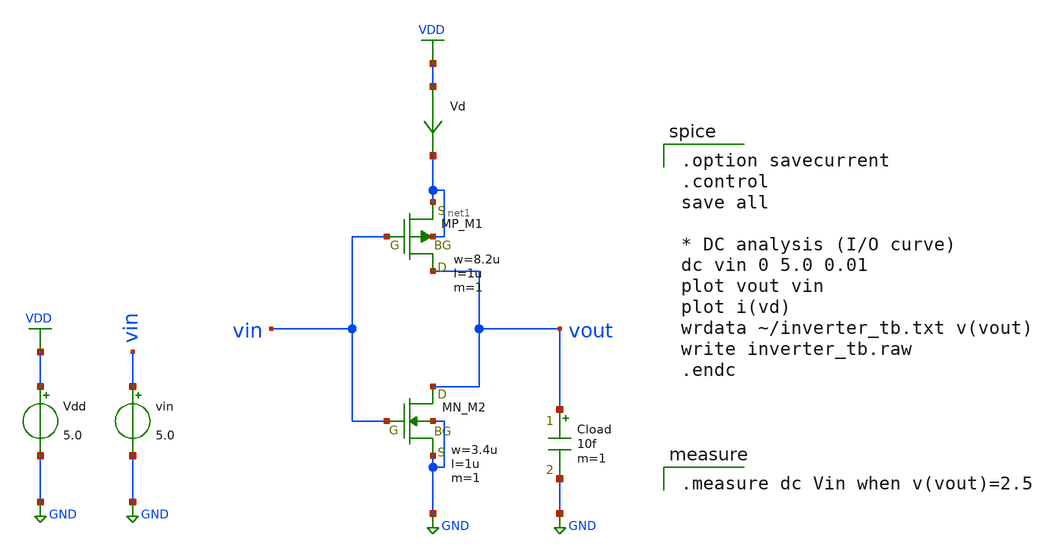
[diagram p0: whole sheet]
** sch_path: member_project/inverter/OpenSUSI/makoto56/inverter_tb.sch
**.subckt inverter_tb
Vdd VDD GND 5.0
vin vin GND 5.0
Vd VDD net1 0
.save i(vd)
Cload vout GND 10f m=1
XM1 vout vin net1 net1 PMOS w=8.2u l=1u as=0 ad=0 ps=0 pd=0 nrd=0 nrs=0 m=1
XM2 vout vin GND GND NMOS w=3.4u l=1u as=0 ad=0 ps=0 pd=0 nrd=0 nrs=0 m=1
**** begin user architecture code

.option savecurrent
.control
save all

* DC analysis (I/O curve)
dc vin 0 5.0 0.01
plot vout vin
plot i(vd)
wrdata ~/inverter_tb.txt v(vout)
write inverter_tb.raw
.endc


.measure dc Vin when v(vout)=2.5

 .include $::LIB/ip62_models
**** end user architecture code
**.ends
.GLOBAL VDD
.GLOBAL GND
.end
